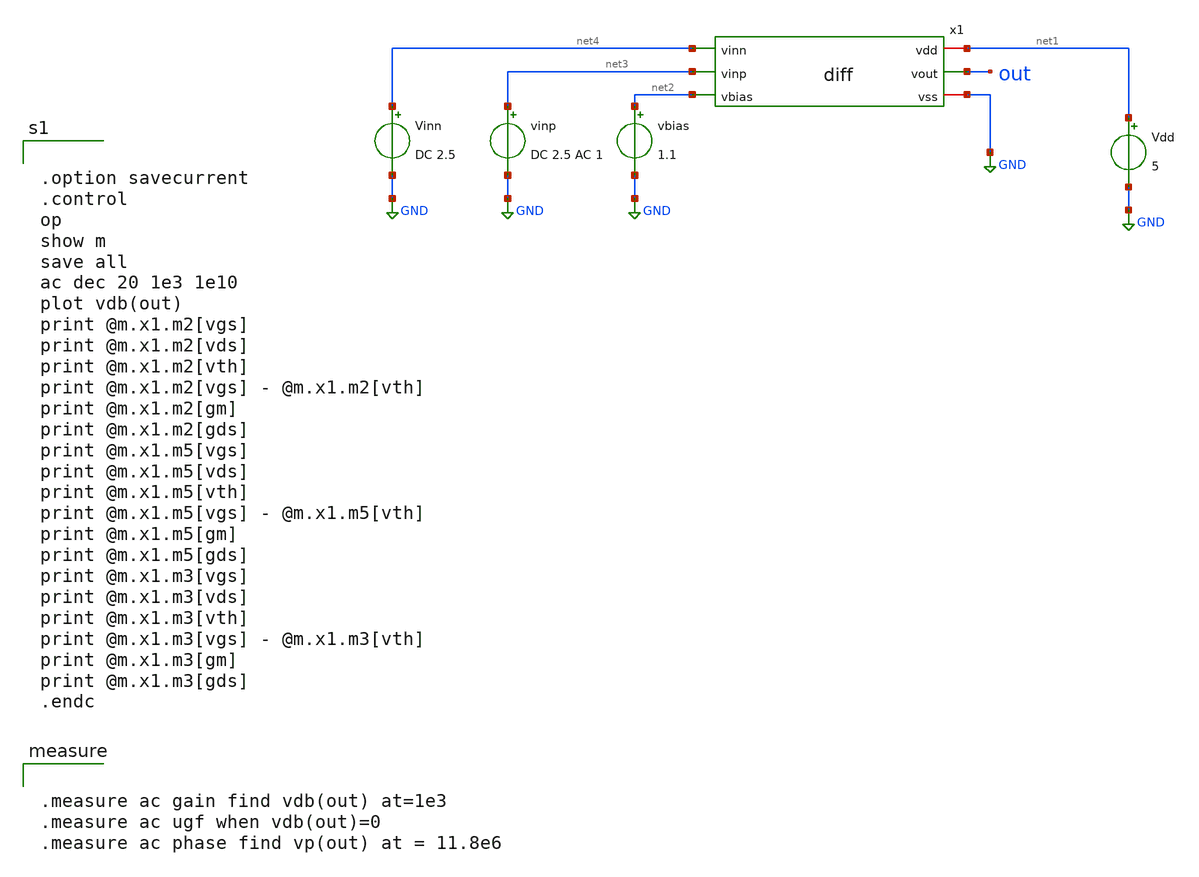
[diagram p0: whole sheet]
** sch_path: member_project/GroupWork/Team_masahiro/diff_ac.sch
**.subckt diff_ac
x1 net1 out net4 net3 net2 GND diff
Vinn net4 GND DC 2.5
vinp net3 GND DC 2.5 AC 1
vbias net2 GND 1.1
Vdd net1 GND 5
**** begin user architecture code
 .include $::LIB/mos.lib
.include $::LIB/passive.lib
.include $::LIB/diode.lib


.option savecurrent
.control
op
show m
save all
ac dec 20 1e3 1e10
plot vdb(out)
print @m.x1.m2[vgs]
print @m.x1.m2[vds]
print @m.x1.m2[vth]
print @m.x1.m2[vgs] - @m.x1.m2[vth]
print @m.x1.m2[gm]
print @m.x1.m2[gds]
print @m.x1.m5[vgs]
print @m.x1.m5[vds]
print @m.x1.m5[vth]
print @m.x1.m5[vgs] - @m.x1.m5[vth]
print @m.x1.m5[gm]
print @m.x1.m5[gds]
print @m.x1.m3[vgs]
print @m.x1.m3[vds]
print @m.x1.m3[vth]
print @m.x1.m3[vgs] - @m.x1.m3[vth]
print @m.x1.m3[gm]
print @m.x1.m3[gds]
.endc




.measure ac gain find vdb(out) at=1e3
.measure ac ugf when vdb(out)=0
.measure ac phase find vp(out) at = 11.8e6


**** end user architecture code
**.ends

* expanding   symbol:  diff.sym # of pins=6
** sym_path: member_project/GroupWork/Team_masahiro/diff.sym
** sch_path: member_project/GroupWork/Team_masahiro/diff.sch
.subckt diff vdd vout vinn vinp vbias vss
*.iopin vss
*.iopin vdd
*.ipin vinn
*.ipin vinp
*.opin vout
*.ipin vbias
M1 net1 vinn net2 vss nmos L=2u W=100u m=1
M2 vout vinp net2 vss nmos L=2u W=100u m=1
M3 net2 vbias vss vss nmos L=2u W=20u m=1
M4 net1 net1 vdd vdd pmos L=2u W=35u m=1
M5 vout net1 vdd vdd pmos L=2u W=35u m=1
.ends

.GLOBAL GND
.end
